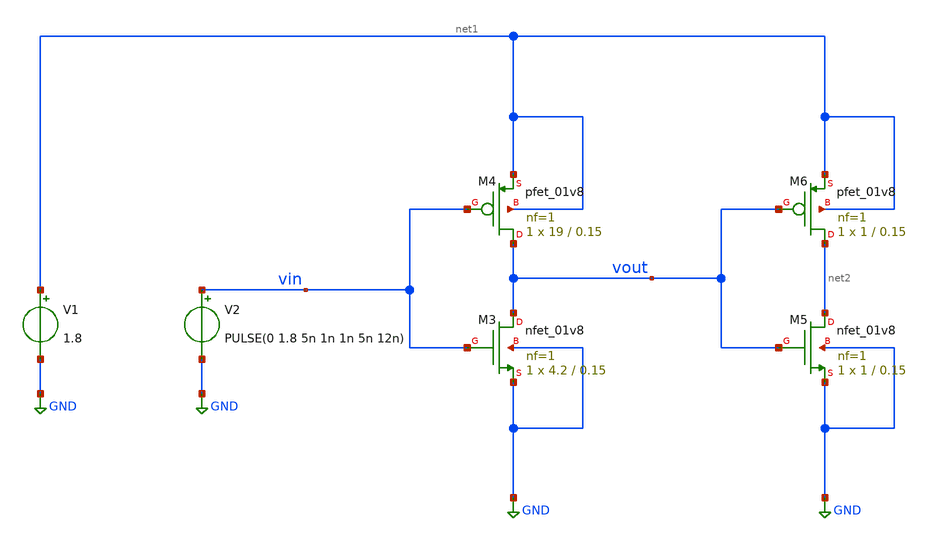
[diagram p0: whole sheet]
** sch_path: TT/tech_char_mobillities.sch
.lib $::SKYWATER_MODELS/sky130.lib.spice tt
.include $::SKYWATER_STDCELLS/sky130_fd_sc_hd.spice

**.subckt tech_char_mobillities
XM3 vout vin GND GND sky130_fd_pr__nfet_01v8 L=0.15 W=4.2 nf=1 ad='int((nf+1)/2) * W/nf * 0.29' as='int((nf+2)/2) * W/nf * 0.29'
+ pd='2*int((nf+1)/2) * (W/nf + 0.29)' ps='2*int((nf+2)/2) * (W/nf + 0.29)' nrd='0.29 / W' nrs='0.29 / W'
+ sa=0 sb=0 sd=0 mult=1 m=1
XM4 vout vin net1 net1 sky130_fd_pr__pfet_01v8 L=0.15 W=19 nf=1 ad='int((nf+1)/2) * W/nf * 0.29' as='int((nf+2)/2) * W/nf * 0.29'
+ pd='2*int((nf+1)/2) * (W/nf + 0.29)' ps='2*int((nf+2)/2) * (W/nf + 0.29)' nrd='0.29 / W' nrs='0.29 / W'
+ sa=0 sb=0 sd=0 mult=1 m=1
XM5 net2 vout GND GND sky130_fd_pr__nfet_01v8 L=0.15 W=1 nf=1 ad='int((nf+1)/2) * W/nf * 0.29' as='int((nf+2)/2) * W/nf * 0.29'
+ pd='2*int((nf+1)/2) * (W/nf + 0.29)' ps='2*int((nf+2)/2) * (W/nf + 0.29)' nrd='0.29 / W' nrs='0.29 / W'
+ sa=0 sb=0 sd=0 mult=1 m=1
XM6 net2 vout net1 net1 sky130_fd_pr__pfet_01v8 L=0.15 W=1 nf=1 ad='int((nf+1)/2) * W/nf * 0.29' as='int((nf+2)/2) * W/nf * 0.29'
+ pd='2*int((nf+1)/2) * (W/nf + 0.29)' ps='2*int((nf+2)/2) * (W/nf + 0.29)' nrd='0.29 / W' nrs='0.29 / W'
+ sa=0 sb=0 sd=0 mult=1 m=1
V1 net1 GND 1.8
V2 vin GND PULSE(0 1.8 5n 1n 1n 5n 12n)
**** begin user architecture code


.tran 0.1n 24n
.save all


**** end user architecture code
**.ends
.GLOBAL GND
.end
